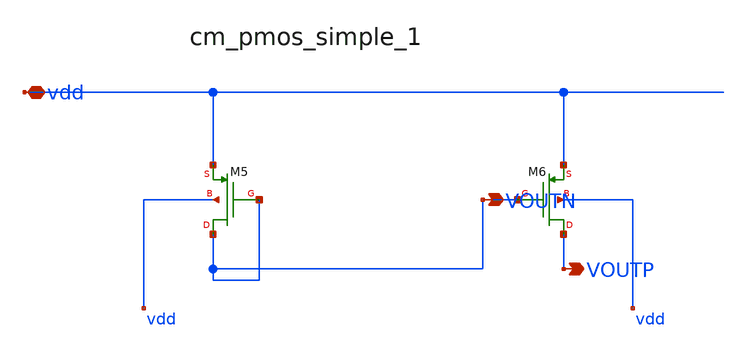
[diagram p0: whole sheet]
** sch_path: analog-db/raw/amp_012_peng_tcfc/hier/blocks/cm_pmos_simple_1.sch
**.subckt cm_pmos_simple_1 vdd VOUTN VOUTP
*.iopin vdd
*.opin VOUTN
*.opin VOUTP
XM5 VOUTN VOUTN vdd vdd sg13_lv_pmos w=x_dut_xm5_w l=x_dut_xm5_l ng=1 m=x_dut_xm5_m
XM6 VOUTP VOUTN vdd vdd sg13_lv_pmos w=x_dut_xm6_w l=x_dut_xm6_l ng=1 m=x_dut_xm6_m
**.ends
.end
